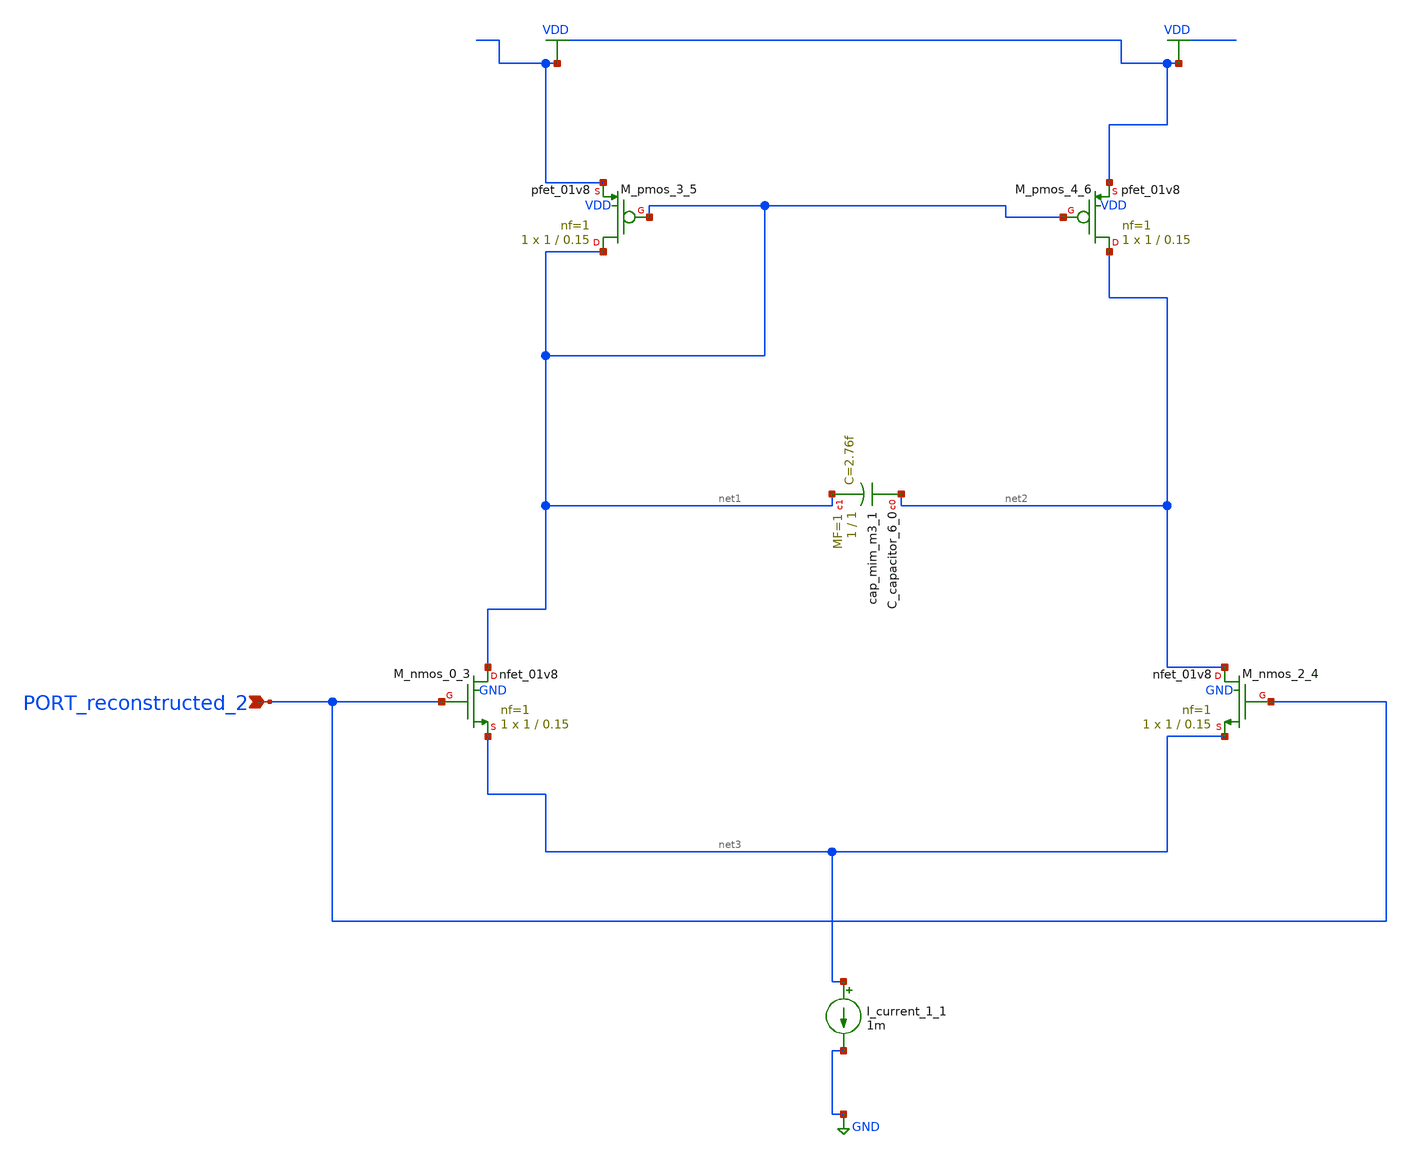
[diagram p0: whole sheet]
** sch_path: schematics/AMSNet/351.sch
**.subckt 351 PORT_reconstructed_2
*.ipin PORT_reconstructed_2
XC_capacitor_6_0 net2 net1 sky130_fd_pr__cap_mim_m3_1 W=1 L=1 MF=1 m=1
I_current_1_1 net3 GND 1m
XM_nmos_0_3 net1 PORT_reconstructed_2 net3 GND sky130_fd_pr__nfet_01v8 L=0.15 W=1 nf=1 ad='int((1 + 1)/2) * 1 / 1 * 0.29'
+ as='int((1 + 2)/2) * 1 / 1 * 0.29' pd='2*int((1 + 1)/2) * (1 / 1 + 0.29)' ps='2*int((1 + 2)/2) * (1 / 1 + 0.29)'
+ nrd='0.29 / 1 ' nrs='0.29 / 1 ' sa=0 sb=0 sd=0 mult=1 m=1
XM_nmos_2_4 net2 PORT_reconstructed_2 net3 GND sky130_fd_pr__nfet_01v8 L=0.15 W=1 nf=1 ad='int((1 + 1)/2) * 1 / 1 * 0.29'
+ as='int((1 + 2)/2) * 1 / 1 * 0.29' pd='2*int((1 + 1)/2) * (1 / 1 + 0.29)' ps='2*int((1 + 2)/2) * (1 / 1 + 0.29)'
+ nrd='0.29 / 1 ' nrs='0.29 / 1 ' sa=0 sb=0 sd=0 mult=1 m=1
XM_pmos_3_5 net1 net1 VDD VDD sky130_fd_pr__pfet_01v8 L=0.15 W=1 nf=1 ad='int((1 + 1)/2) * 1 / 1 * 0.29'
+ as='int((1 + 2)/2) * 1 / 1 * 0.29' pd='2*int((1 + 1)/2) * (1 / 1 + 0.29)' ps='2*int((1 + 2)/2) * (1 / 1 + 0.29)'
+ nrd='0.29 / 1 ' nrs='0.29 / 1 ' sa=0 sb=0 sd=0 mult=1 m=1
XM_pmos_4_6 net2 net1 VDD VDD sky130_fd_pr__pfet_01v8 L=0.15 W=1 nf=1 ad='int((1 + 1)/2) * 1 / 1 * 0.29'
+ as='int((1 + 2)/2) * 1 / 1 * 0.29' pd='2*int((1 + 1)/2) * (1 / 1 + 0.29)' ps='2*int((1 + 2)/2) * (1 / 1 + 0.29)'
+ nrd='0.29 / 1 ' nrs='0.29 / 1 ' sa=0 sb=0 sd=0 mult=1 m=1
**.ends
.GLOBAL GND
.GLOBAL VDD
.end
